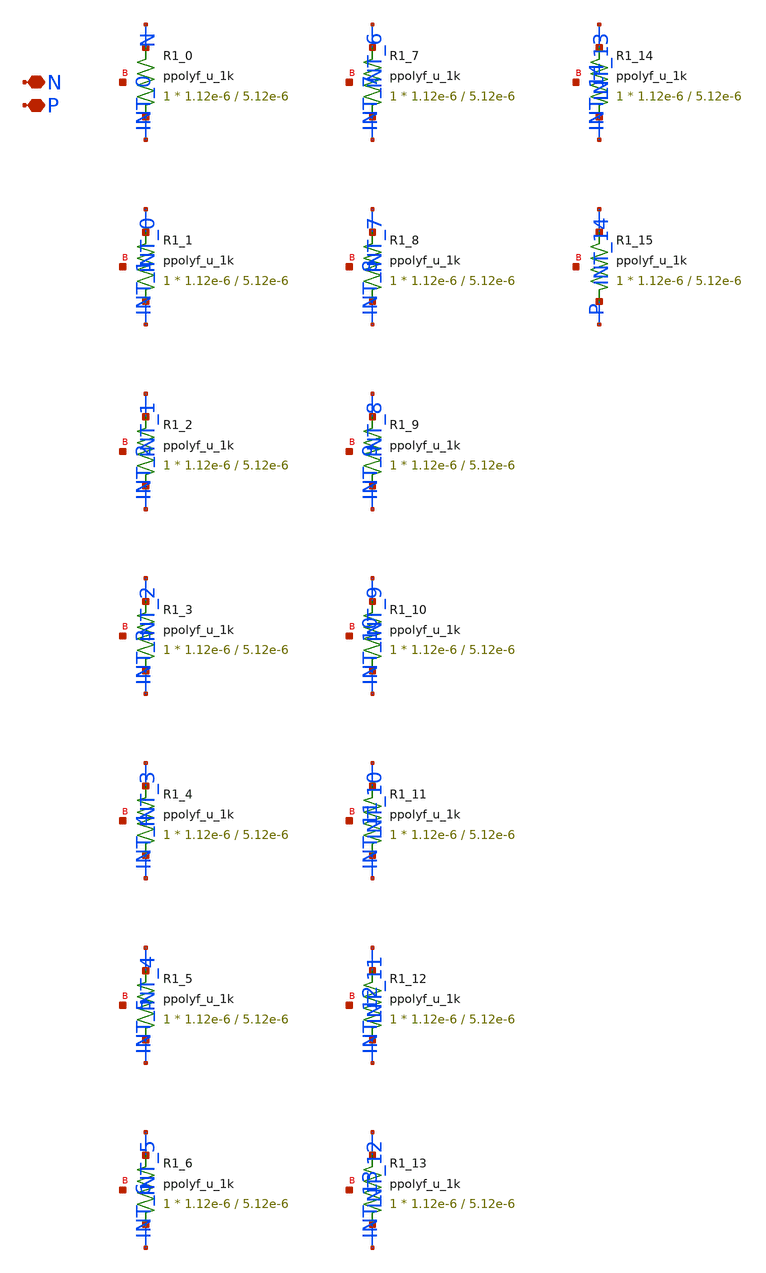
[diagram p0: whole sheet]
** sch_path: design/LELO_TR_GF180MCUD/LELOTR_RES16.sch
**.subckt LELOTR_RES16 N P
*.iopin N
*.iopin P
XR1_0 INT_0 N net1 ppolyf_u_1k r_width=1.12e-6 r_length=5.12e-6 m=1
XR1_1 INT_1 INT_0 net2 ppolyf_u_1k r_width=1.12e-6 r_length=5.12e-6 m=1
XR1_2 INT_2 INT_1 net3 ppolyf_u_1k r_width=1.12e-6 r_length=5.12e-6 m=1
XR1_3 INT_3 INT_2 net4 ppolyf_u_1k r_width=1.12e-6 r_length=5.12e-6 m=1
XR1_4 INT_4 INT_3 net5 ppolyf_u_1k r_width=1.12e-6 r_length=5.12e-6 m=1
XR1_5 INT_5 INT_4 net6 ppolyf_u_1k r_width=1.12e-6 r_length=5.12e-6 m=1
XR1_6 INT_6 INT_5 net7 ppolyf_u_1k r_width=1.12e-6 r_length=5.12e-6 m=1
XR1_7 INT_7 INT_6 net8 ppolyf_u_1k r_width=1.12e-6 r_length=5.12e-6 m=1
XR1_8 INT_8 INT_7 net9 ppolyf_u_1k r_width=1.12e-6 r_length=5.12e-6 m=1
XR1_9 INT_9 INT_8 net10 ppolyf_u_1k r_width=1.12e-6 r_length=5.12e-6 m=1
XR1_10 INT_10 INT_9 net11 ppolyf_u_1k r_width=1.12e-6 r_length=5.12e-6 m=1
XR1_11 INT_11 INT_10 net12 ppolyf_u_1k r_width=1.12e-6 r_length=5.12e-6 m=1
XR1_12 INT_12 INT_11 net13 ppolyf_u_1k r_width=1.12e-6 r_length=5.12e-6 m=1
XR1_13 INT_13 INT_12 net14 ppolyf_u_1k r_width=1.12e-6 r_length=5.12e-6 m=1
XR1_14 INT_14 INT_13 net15 ppolyf_u_1k r_width=1.12e-6 r_length=5.12e-6 m=1
XR1_15 P INT_14 net16 ppolyf_u_1k r_width=1.12e-6 r_length=5.12e-6 m=1
**.ends
.end
